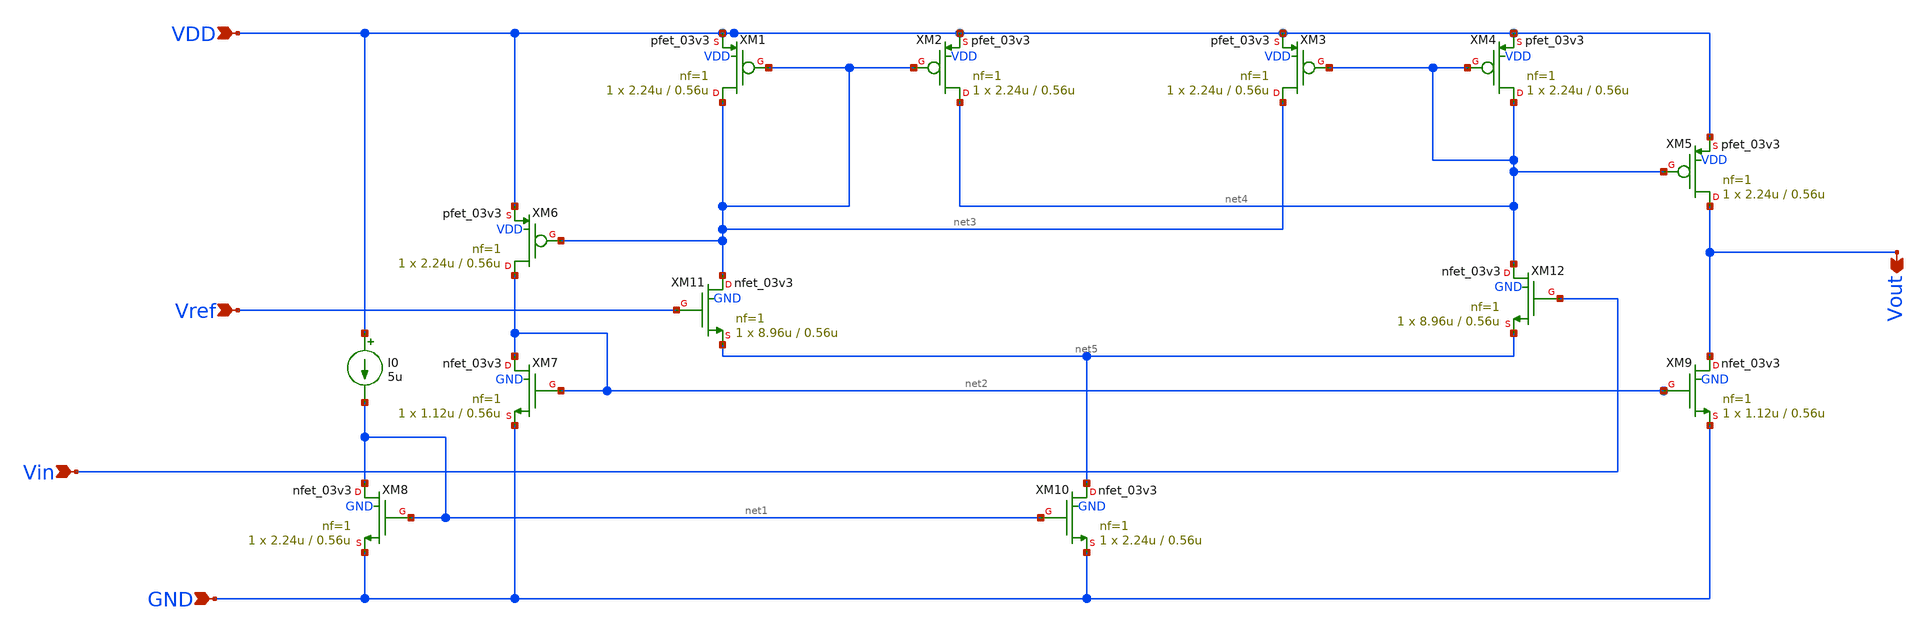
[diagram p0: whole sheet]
** sch_path: comparator/schematic-design/comp_forsym.sch
**.subckt comp_forsym Vout Vref Vin VDD GND
*.opin Vout
*.ipin Vref
*.ipin Vin
*.ipin VDD
*.ipin GND
XM1 net3 net3 VDD VDD pfet_03v3 L=0.56u W=2.24u nf=1 ad='int((nf+1)/2) * W/nf * 0.18u' as='int((nf+2)/2) * W/nf * 0.18u'
+ pd='2*int((nf+1)/2) * (W/nf + 0.18u)' ps='2*int((nf+2)/2) * (W/nf + 0.18u)' nrd='0.18u / W' nrs='0.18u / W'
+ sa=0 sb=0 sd=0 m=1 par=1
XM2 net4 net3 VDD VDD pfet_03v3 L=0.56u W=2.24u nf=1 ad='int((nf+1)/2) * W/nf * 0.18u' as='int((nf+2)/2) * W/nf * 0.18u'
+ pd='2*int((nf+1)/2) * (W/nf + 0.18u)' ps='2*int((nf+2)/2) * (W/nf + 0.18u)' nrd='0.18u / W' nrs='0.18u / W'
+ sa=0 sb=0 sd=0 m=1 par=1
XM3 net3 net4 VDD VDD pfet_03v3 L=0.56u W=2.24u nf=1 ad='int((nf+1)/2) * W/nf * 0.18u' as='int((nf+2)/2) * W/nf * 0.18u'
+ pd='2*int((nf+1)/2) * (W/nf + 0.18u)' ps='2*int((nf+2)/2) * (W/nf + 0.18u)' nrd='0.18u / W' nrs='0.18u / W'
+ sa=0 sb=0 sd=0 m=1 par=1
XM4 net4 net4 VDD VDD pfet_03v3 L=0.56u W=2.24u nf=1 ad='int((nf+1)/2) * W/nf * 0.18u' as='int((nf+2)/2) * W/nf * 0.18u'
+ pd='2*int((nf+1)/2) * (W/nf + 0.18u)' ps='2*int((nf+2)/2) * (W/nf + 0.18u)' nrd='0.18u / W' nrs='0.18u / W'
+ sa=0 sb=0 sd=0 m=1 par=1
XM5 Vout net4 VDD VDD pfet_03v3 L=0.56u W=2.24u nf=1 ad='int((nf+1)/2) * W/nf * 0.18u' as='int((nf+2)/2) * W/nf * 0.18u'
+ pd='2*int((nf+1)/2) * (W/nf + 0.18u)' ps='2*int((nf+2)/2) * (W/nf + 0.18u)' nrd='0.18u / W' nrs='0.18u / W'
+ sa=0 sb=0 sd=0 m=1 par=1
XM6 net2 net3 VDD VDD pfet_03v3 L=0.56u W=2.24u nf=1 ad='int((nf+1)/2) * W/nf * 0.18u' as='int((nf+2)/2) * W/nf * 0.18u'
+ pd='2*int((nf+1)/2) * (W/nf + 0.18u)' ps='2*int((nf+2)/2) * (W/nf + 0.18u)' nrd='0.18u / W' nrs='0.18u / W'
+ sa=0 sb=0 sd=0 m=1 par=1
XM7 net2 net2 GND GND nfet_03v3 L=0.56u W=1.12u nf=1 ad='int((nf+1)/2) * W/nf * 0.18u' as='int((nf+2)/2) * W/nf * 0.18u'
+ pd='2*int((nf+1)/2) * (W/nf + 0.18u)' ps='2*int((nf+2)/2) * (W/nf + 0.18u)' nrd='0.18u / W' nrs='0.18u / W'
+ sa=0 sb=0 sd=0 m=1 par=1
XM8 net1 net1 GND GND nfet_03v3 L=0.56u W=2.24u nf=1 ad='int((nf+1)/2) * W/nf * 0.18u' as='int((nf+2)/2) * W/nf * 0.18u'
+ pd='2*int((nf+1)/2) * (W/nf + 0.18u)' ps='2*int((nf+2)/2) * (W/nf + 0.18u)' nrd='0.18u / W' nrs='0.18u / W'
+ sa=0 sb=0 sd=0 m=1 par=1
XM9 Vout net2 GND GND nfet_03v3 L=0.56u W=1.12u nf=1 ad='int((nf+1)/2) * W/nf * 0.18u' as='int((nf+2)/2) * W/nf * 0.18u'
+ pd='2*int((nf+1)/2) * (W/nf + 0.18u)' ps='2*int((nf+2)/2) * (W/nf + 0.18u)' nrd='0.18u / W' nrs='0.18u / W'
+ sa=0 sb=0 sd=0 m=1 par=1
XM10 net5 net1 GND GND nfet_03v3 L=0.56u W=2.24u nf=1 ad='int((nf+1)/2) * W/nf * 0.18u' as='int((nf+2)/2) * W/nf * 0.18u'
+ pd='2*int((nf+1)/2) * (W/nf + 0.18u)' ps='2*int((nf+2)/2) * (W/nf + 0.18u)' nrd='0.18u / W' nrs='0.18u / W'
+ sa=0 sb=0 sd=0 m=1 par=1
XM11 net3 Vref net5 GND nfet_03v3 L=0.56u W=8.96u nf=1 ad='int((nf+1)/2) * W/nf * 0.18u' as='int((nf+2)/2) * W/nf * 0.18u'
+ pd='2*int((nf+1)/2) * (W/nf + 0.18u)' ps='2*int((nf+2)/2) * (W/nf + 0.18u)' nrd='0.18u / W' nrs='0.18u / W'
+ sa=0 sb=0 sd=0 m=1 par=1
XM12 net4 Vin net5 GND nfet_03v3 L=0.56u W=8.96u nf=1 ad='int((nf+1)/2) * W/nf * 0.18u' as='int((nf+2)/2) * W/nf * 0.18u'
+ pd='2*int((nf+1)/2) * (W/nf + 0.18u)' ps='2*int((nf+2)/2) * (W/nf + 0.18u)' nrd='0.18u / W' nrs='0.18u / W'
+ sa=0 sb=0 sd=0 m=1 par=1
I0 VDD net1 5u
**.ends
.end
